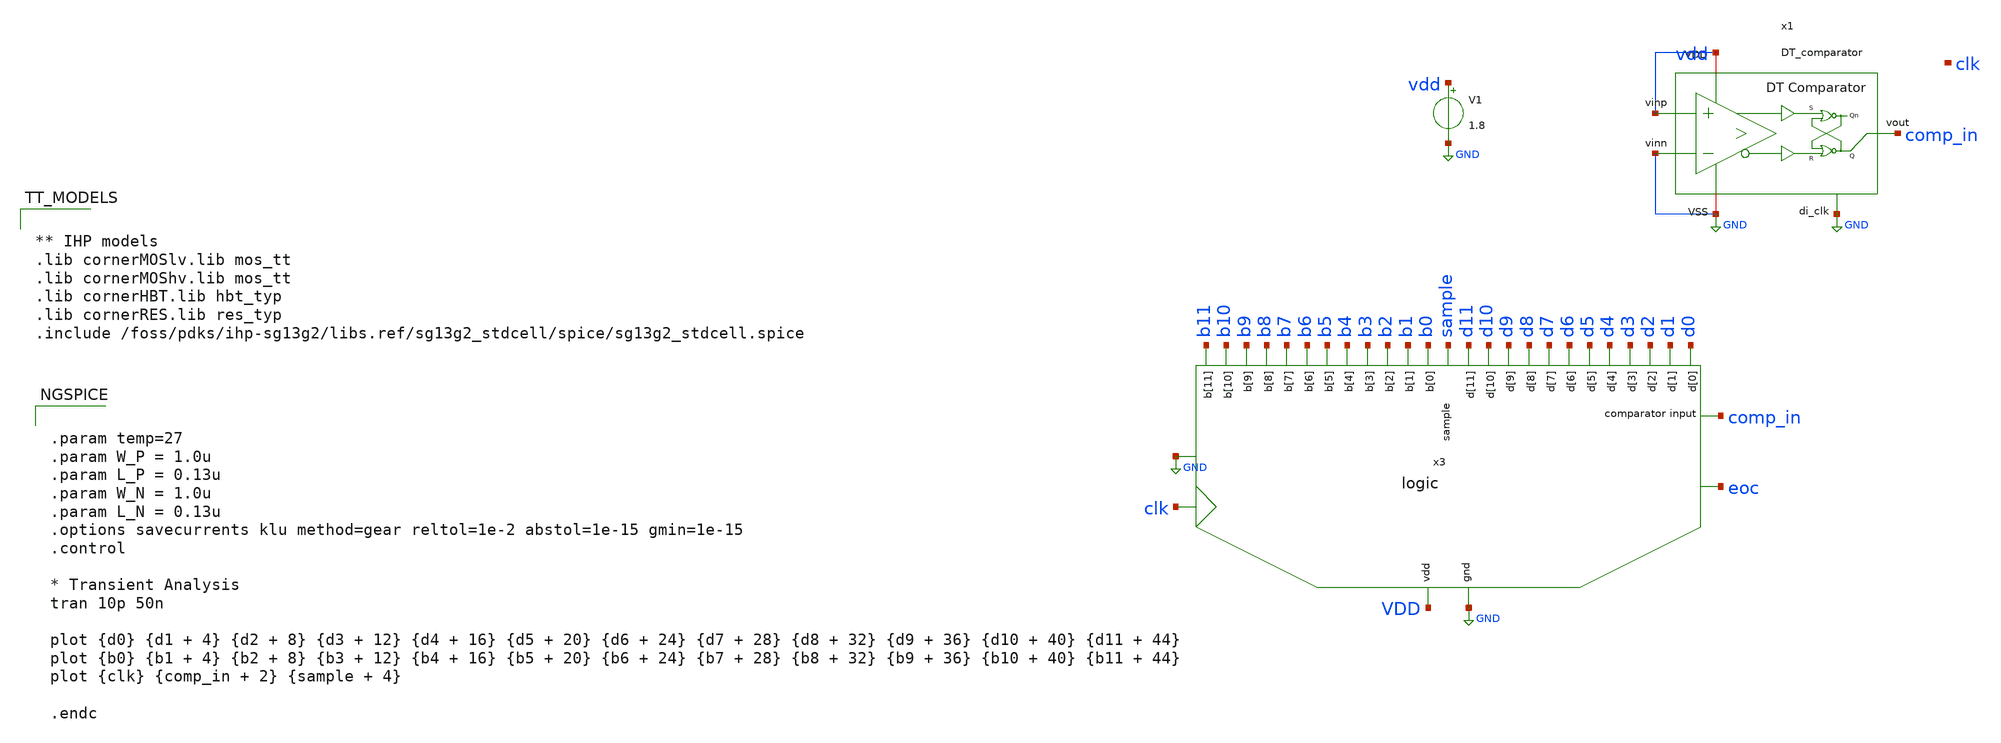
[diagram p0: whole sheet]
** sch_path: xschem/logic/testbench/tb_logic_comp_clk.sch
**.subckt tb_logic_comp_clk
x3 b9 b7 b0 b11 b3 b4 b2 b1 b8 b6 b5 b10 GND VDD sample d9 d7 d0 d11 d3 d4 d2 d1 d8 d6 d5 d10
+ comp_in clk GND eoc logic
V1 vdd GND 1.8
x1 vdd vdd comp_in GND GND GND clk DT_comparator
**** begin user architecture code


.param temp=27
.param W_P = 1.0u
.param L_P = 0.13u
.param W_N = 1.0u
.param L_N = 0.13u
.options savecurrents klu method=gear reltol=1e-2 abstol=1e-15 gmin=1e-15
.control

* Transient Analysis
tran 10p 50n

plot {d0} {d1 + 4} {d2 + 8} {d3 + 12} {d4 + 16} {d5 + 20} {d6 + 24} {d7 + 28} {d8 + 32} {d9 + 36} {d10 + 40}
+ {d11 + 44}
plot {b0} {b1 + 4} {b2 + 8} {b3 + 12} {b4 + 16} {b5 + 20} {b6 + 24} {b7 + 28} {b8 + 32} {b9 + 36} {b10 + 40}
+ {b11 + 44}
plot {clk} {comp_in + 2} {sample + 4}

.endc




** IHP models
.lib cornerMOSlv.lib mos_tt
.lib cornerMOShv.lib mos_tt
.lib cornerHBT.lib hbt_typ
.lib cornerRES.lib res_typ
.include /foss/pdks/ihp-sg13g2/libs.ref/sg13g2_stdcell/spice/sg13g2_stdcell.spice


**** end user architecture code
**.ends
.GLOBAL GND
.end
